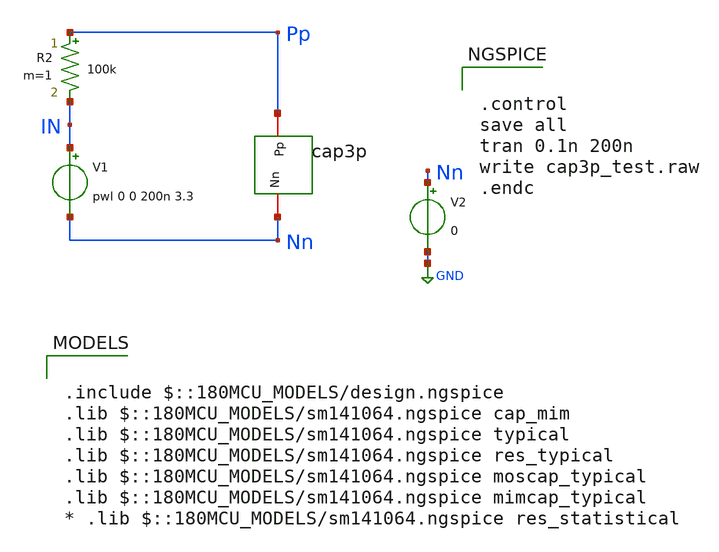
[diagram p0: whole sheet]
** sch_path: Clock_Generator_PAKISTAN_02/Schematics/cap3p_test.sch
**.subckt cap3p_test
V1 IN Nn pwl 0 0 200n 3.3
R2 Pp IN 100k m=1
V2 Nn GND 0
x1 Nn Pp cap3p
**** begin user architecture code

.include $::180MCU_MODELS/design.ngspice
.lib $::180MCU_MODELS/sm141064.ngspice cap_mim
.lib $::180MCU_MODELS/sm141064.ngspice typical
.lib $::180MCU_MODELS/sm141064.ngspice res_typical
.lib $::180MCU_MODELS/sm141064.ngspice moscap_typical
.lib $::180MCU_MODELS/sm141064.ngspice mimcap_typical
* .lib $::180MCU_MODELS/sm141064.ngspice res_statistical



.control
save all
tran 0.1n 200n
write cap3p_test.raw
.endc


**** end user architecture code
**.ends

* expanding   symbol:  cap3p.sym # of pins=2
** sym_path: Clock_Generator_PAKISTAN_02/Schematics/cap3p.sym
** sch_path: Clock_Generator_PAKISTAN_02/Schematics/cap3p.sch
.subckt cap3p Nn Pp
*.iopin Pp
*.iopin Nn
XC1 Pp Nn cap_mim_2f0_m4m5_noshield c_width=42.5e-6 c_length=42.5e-6 m=1
.ends

.GLOBAL GND
.end
